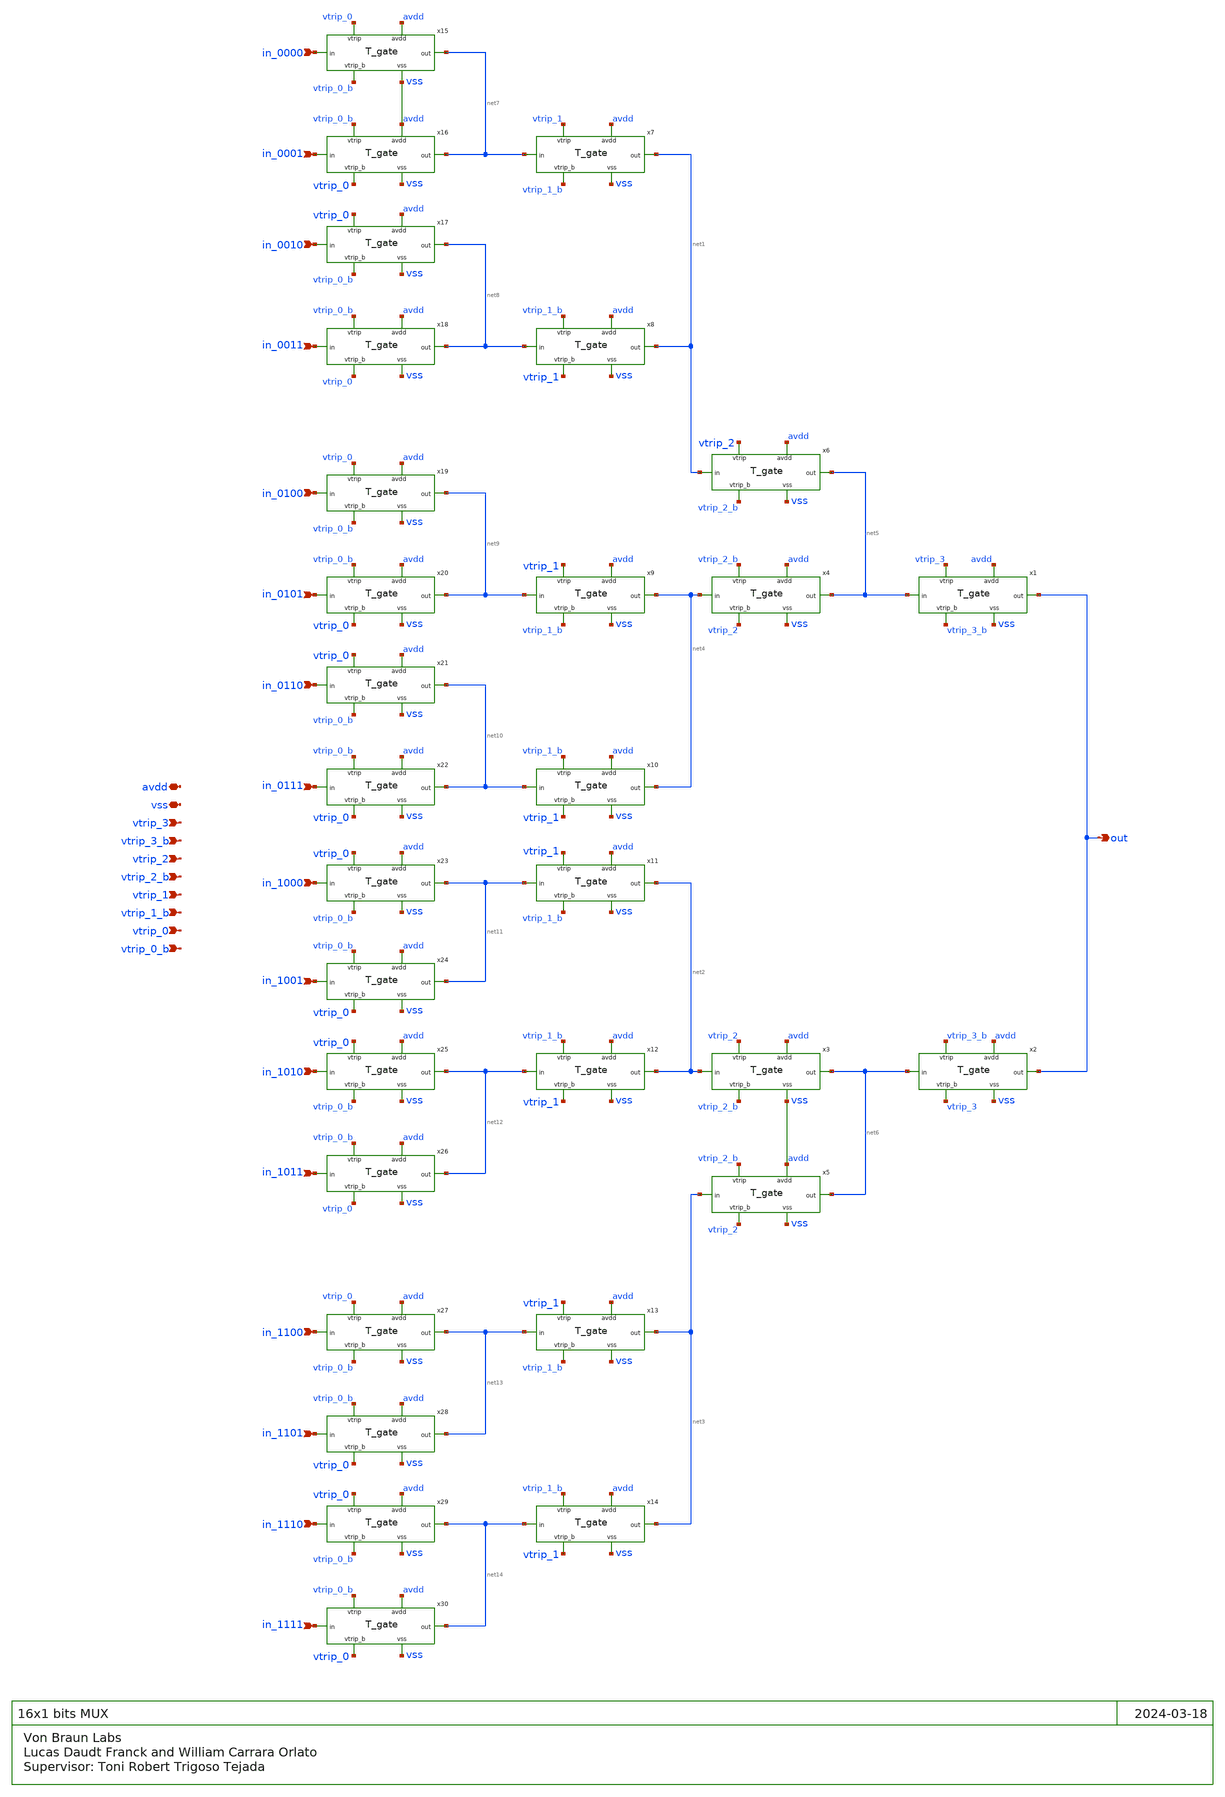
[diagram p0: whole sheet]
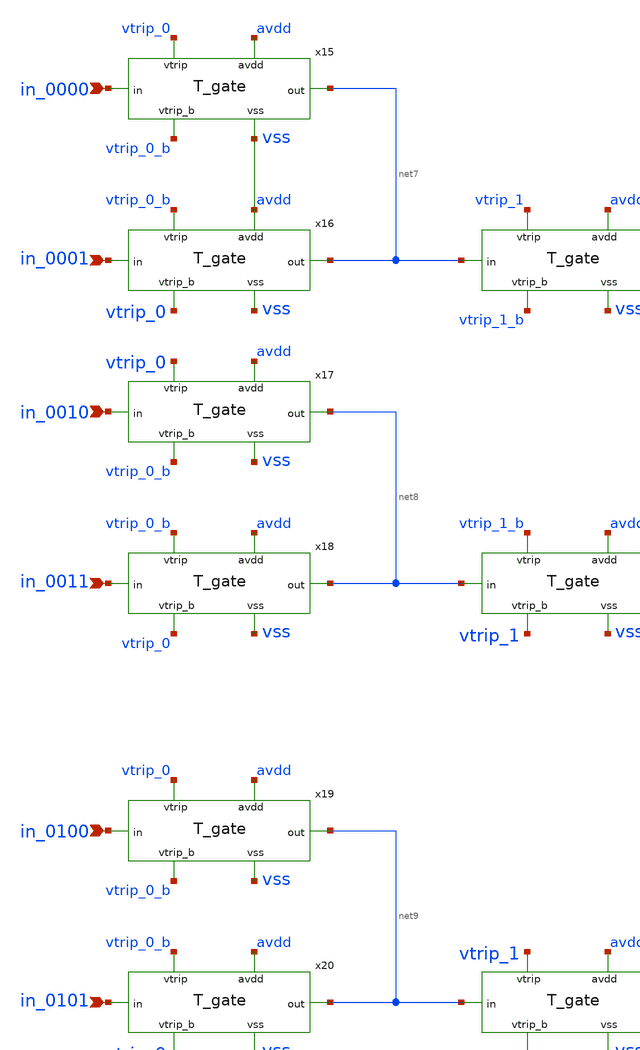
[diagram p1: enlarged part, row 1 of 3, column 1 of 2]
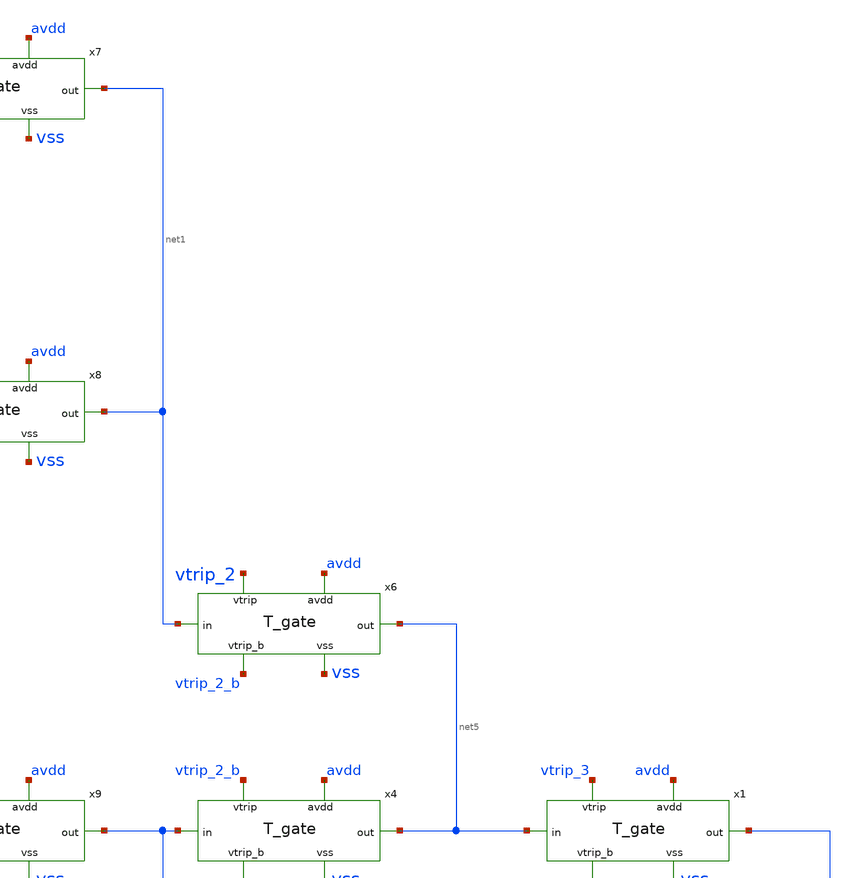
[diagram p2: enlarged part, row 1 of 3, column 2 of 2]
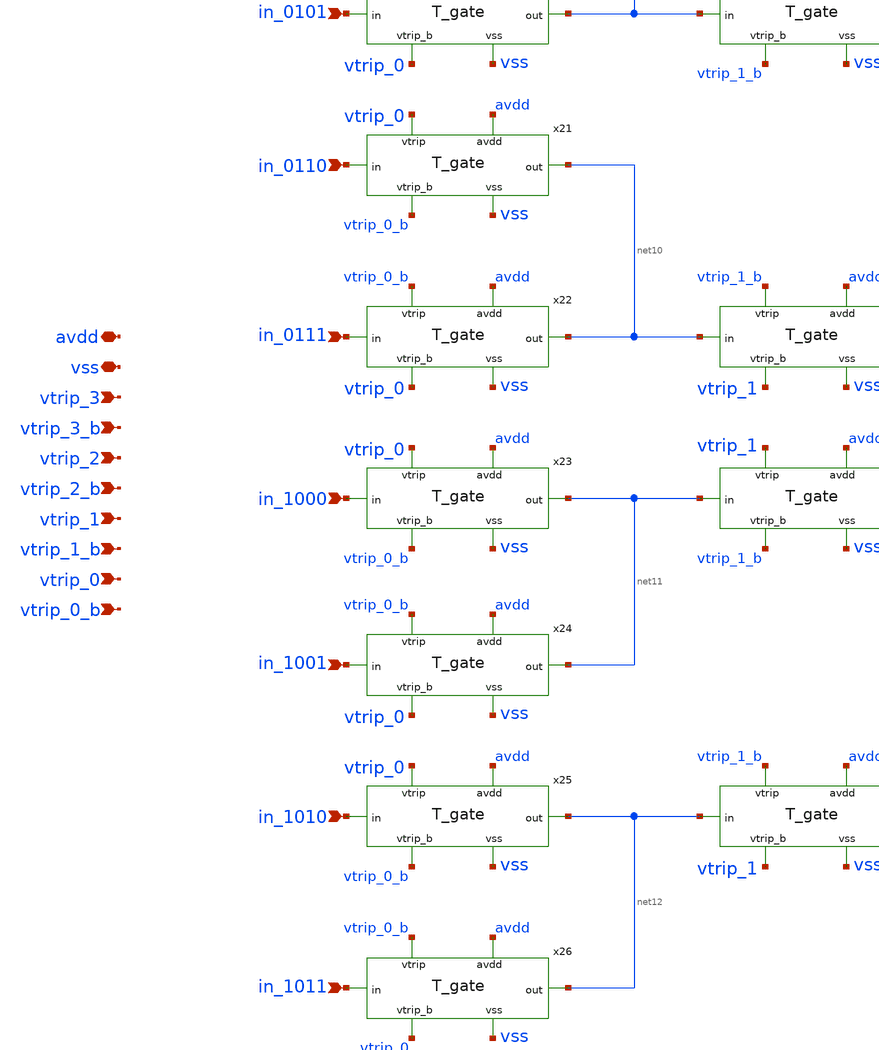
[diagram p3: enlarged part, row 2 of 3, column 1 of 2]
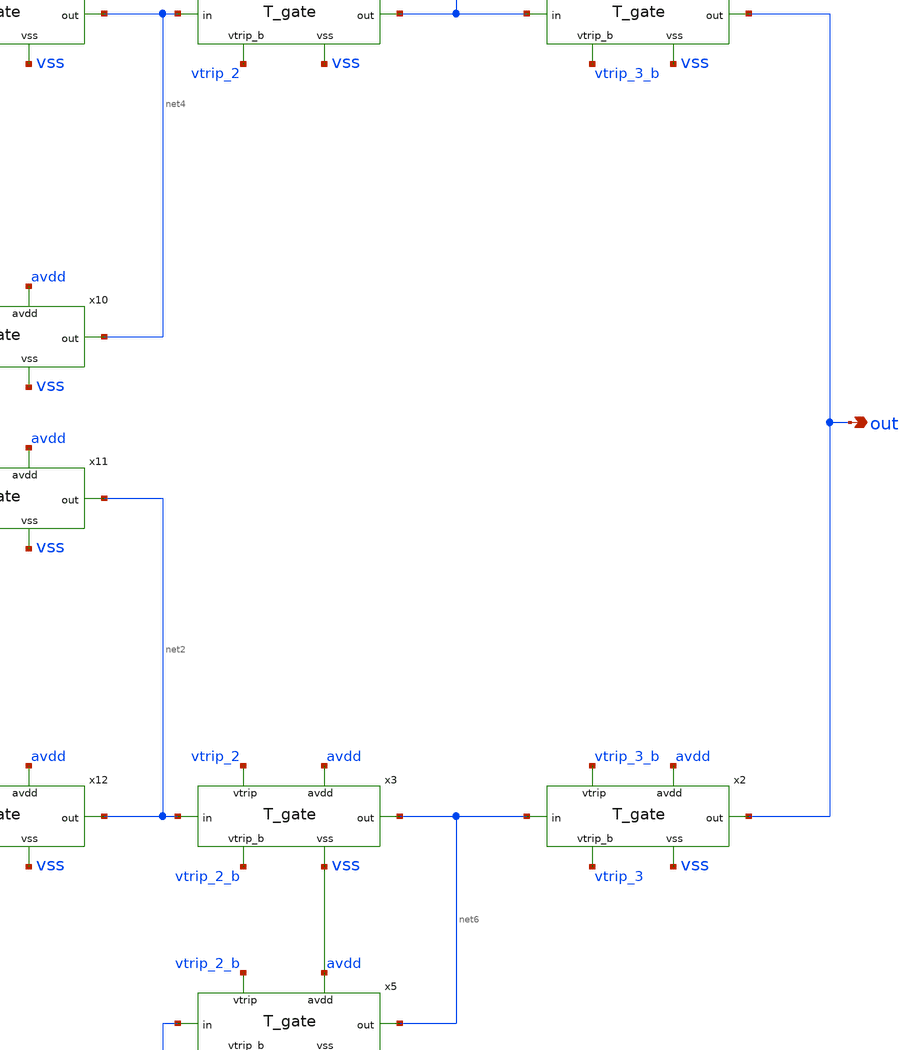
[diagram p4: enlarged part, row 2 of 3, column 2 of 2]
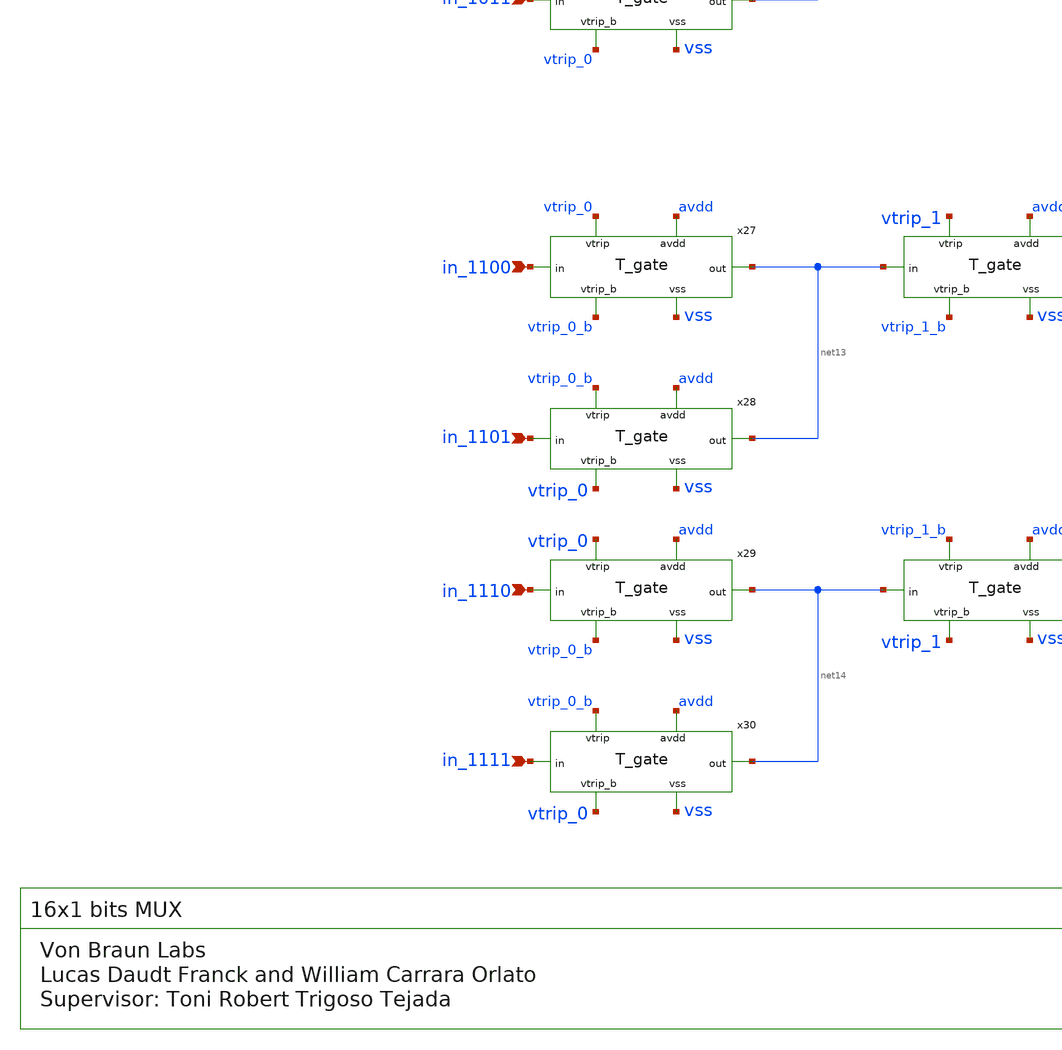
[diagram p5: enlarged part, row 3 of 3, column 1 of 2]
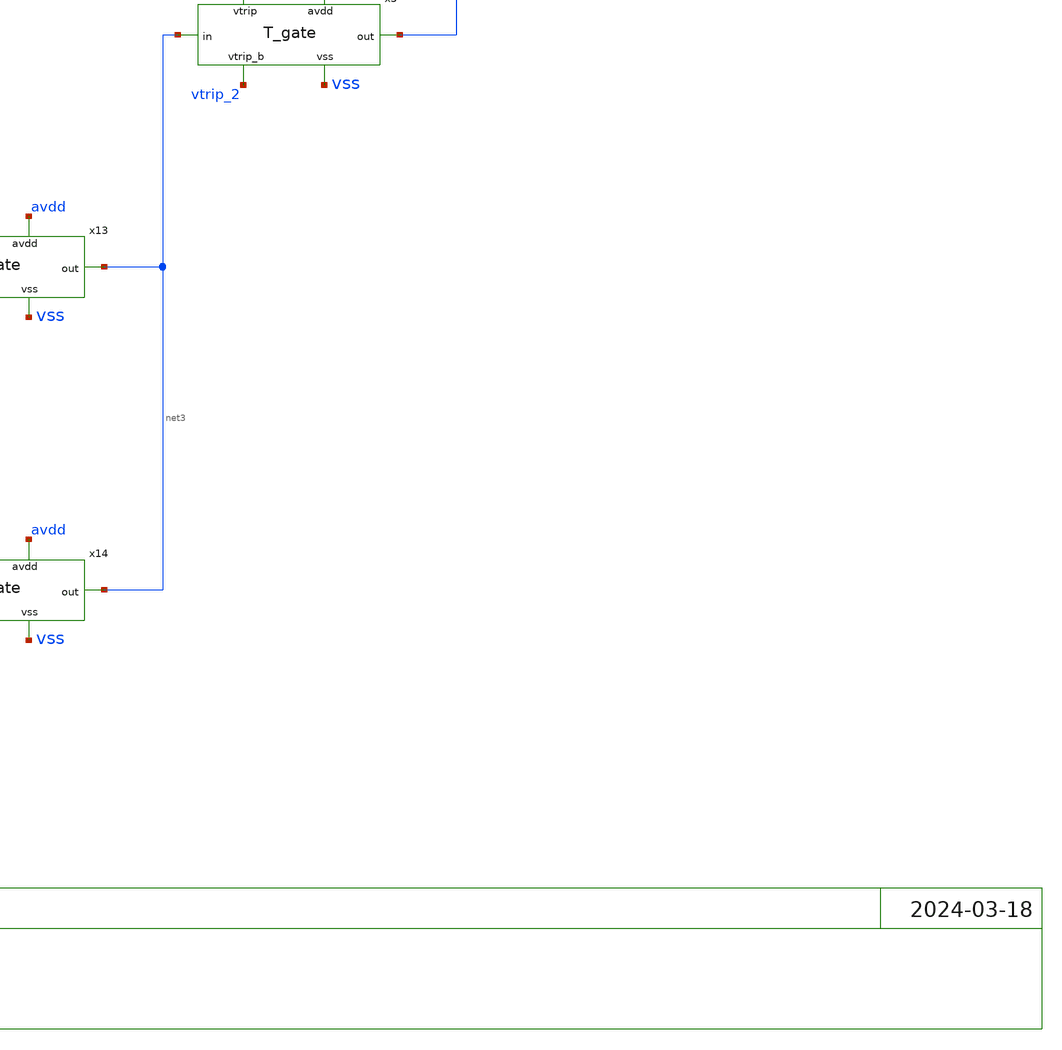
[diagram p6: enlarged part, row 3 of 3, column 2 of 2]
** sch_path: blocks/input/xschem/DemuxCompleto.sch
**.subckt DemuxCompleto in_0000 in_0001 in_0010 in_0011 in_0100 in_0101 in_0110 in_0111 in_1000
*+ in_1001 in_1010 in_1011 in_1110 in_1111 in_1100 in_1101 out vtrip_3 vtrip_3_b vtrip_2 vtrip_2_b vtrip_1
*+ vtrip_1_b vtrip_0 vtrip_0_b avdd vss
*.ipin in_0000
*.ipin in_0001
*.ipin in_0010
*.ipin in_0011
*.ipin in_0100
*.ipin in_0101
*.ipin in_0110
*.ipin in_0111
*.ipin in_1000
*.ipin in_1001
*.ipin in_1010
*.ipin in_1011
*.ipin in_1110
*.ipin in_1111
*.ipin in_1100
*.ipin in_1101
*.opin out
*.ipin vtrip_3
*.ipin vtrip_3_b
*.ipin vtrip_2
*.ipin vtrip_2_b
*.ipin vtrip_1
*.ipin vtrip_1_b
*.ipin vtrip_0
*.ipin vtrip_0_b
*.iopin avdd
*.iopin vss
x1 vtrip_3 avdd net5 out vss vtrip_3_b T_gate
x2 vtrip_3_b avdd net6 out vss vtrip_3 T_gate
x3 vtrip_2 avdd net2 net6 vss vtrip_2_b T_gate
x4 vtrip_2_b avdd net4 net5 vss vtrip_2 T_gate
x5 vtrip_2_b avdd net3 net6 vss vtrip_2 T_gate
x6 vtrip_2 avdd net1 net5 vss vtrip_2_b T_gate
x7 vtrip_1 avdd net7 net1 vss vtrip_1_b T_gate
x8 vtrip_1_b avdd net8 net1 vss vtrip_1 T_gate
x9 vtrip_1 avdd net9 net4 vss vtrip_1_b T_gate
x10 vtrip_1_b avdd net10 net4 vss vtrip_1 T_gate
x11 vtrip_1 avdd net11 net2 vss vtrip_1_b T_gate
x12 vtrip_1_b avdd net12 net2 vss vtrip_1 T_gate
x13 vtrip_1 avdd net13 net3 vss vtrip_1_b T_gate
x14 vtrip_1_b avdd net14 net3 vss vtrip_1 T_gate
x15 vtrip_0 avdd in_0000 net7 vss vtrip_0_b T_gate
x16 vtrip_0_b avdd in_0001 net7 vss vtrip_0 T_gate
x17 vtrip_0 avdd in_0010 net8 vss vtrip_0_b T_gate
x18 vtrip_0_b avdd in_0011 net8 vss vtrip_0 T_gate
x19 vtrip_0 avdd in_0100 net9 vss vtrip_0_b T_gate
x20 vtrip_0_b avdd in_0101 net9 vss vtrip_0 T_gate
x21 vtrip_0 avdd in_0110 net10 vss vtrip_0_b T_gate
x22 vtrip_0_b avdd in_0111 net10 vss vtrip_0 T_gate
x23 vtrip_0 avdd in_1000 net11 vss vtrip_0_b T_gate
x24 vtrip_0_b avdd in_1001 net11 vss vtrip_0 T_gate
x25 vtrip_0 avdd in_1010 net12 vss vtrip_0_b T_gate
x26 vtrip_0_b avdd in_1011 net12 vss vtrip_0 T_gate
x27 vtrip_0 avdd in_1100 net13 vss vtrip_0_b T_gate
x28 vtrip_0_b avdd in_1101 net13 vss vtrip_0 T_gate
x29 vtrip_0 avdd in_1110 net14 vss vtrip_0_b T_gate
x30 vtrip_0_b avdd in_1111 net14 vss vtrip_0 T_gate
**.ends
.end
